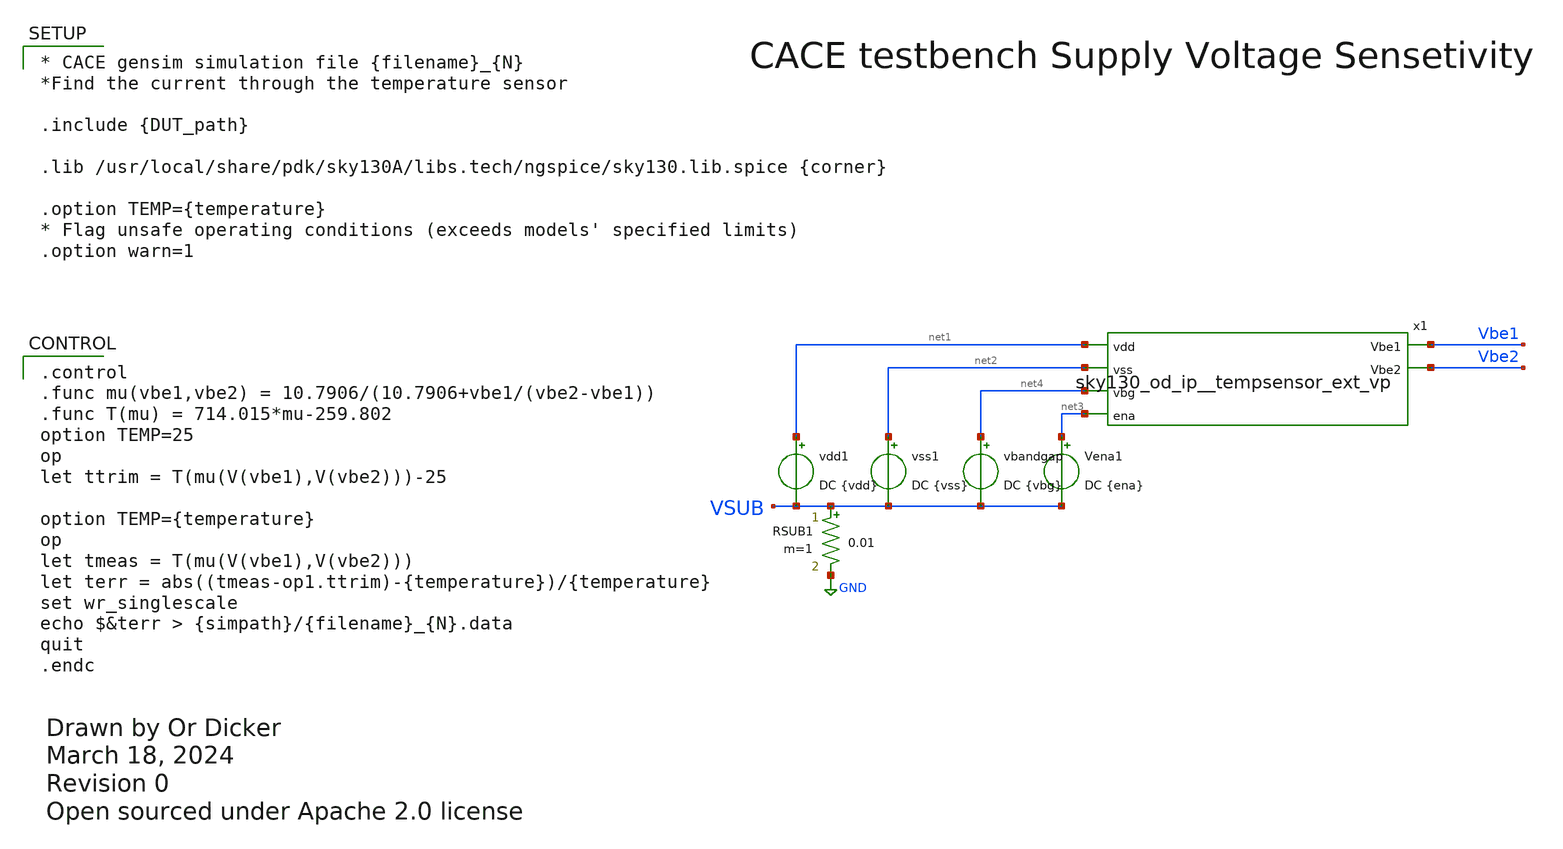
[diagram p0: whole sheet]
** sch_path: cace/templates/supply_sens.sch
* Open sourced under Apache 2.0 license
**.subckt supply_sens
vss1 net2 VSUB DC {vss}
vdd1 net1 VSUB DC {vdd}
RSUB1 VSUB GND 0.01 m=1
Vena1 net3 VSUB DC {ena}
x1 net1 net2 net4 Vbe1 Vbe2 net3 sky130_od_ip__tempsensor_ext_vp
vbandgap net4 VSUB DC {vbg}
**** begin user architecture code

.control
.func mu(vbe1,vbe2) = 10.7906/(10.7906+vbe1/(vbe2-vbe1))
.func T(mu) = 714.015*mu-259.802
option TEMP=25
op
let ttrim = T(mu(V(vbe1),V(vbe2)))-25

option TEMP={temperature}
op
let tmeas = T(mu(V(vbe1),V(vbe2)))
let terr = abs((tmeas-op1.ttrim)-{temperature})/{temperature}
set wr_singlescale
echo $&terr > {simpath}/{filename}_{N}.data
quit
.endc



* CACE gensim simulation file {filename}_{N}
*Find the current through the temperature sensor

.include {DUT_path}

.lib /usr/local/share/pdk/sky130A/libs.tech/ngspice/sky130.lib.spice {corner}

.option TEMP={temperature}
* Flag unsafe operating conditions (exceeds models' specified limits)
.option warn=1


**** end user architecture code
**.ends
.GLOBAL GND
.end
